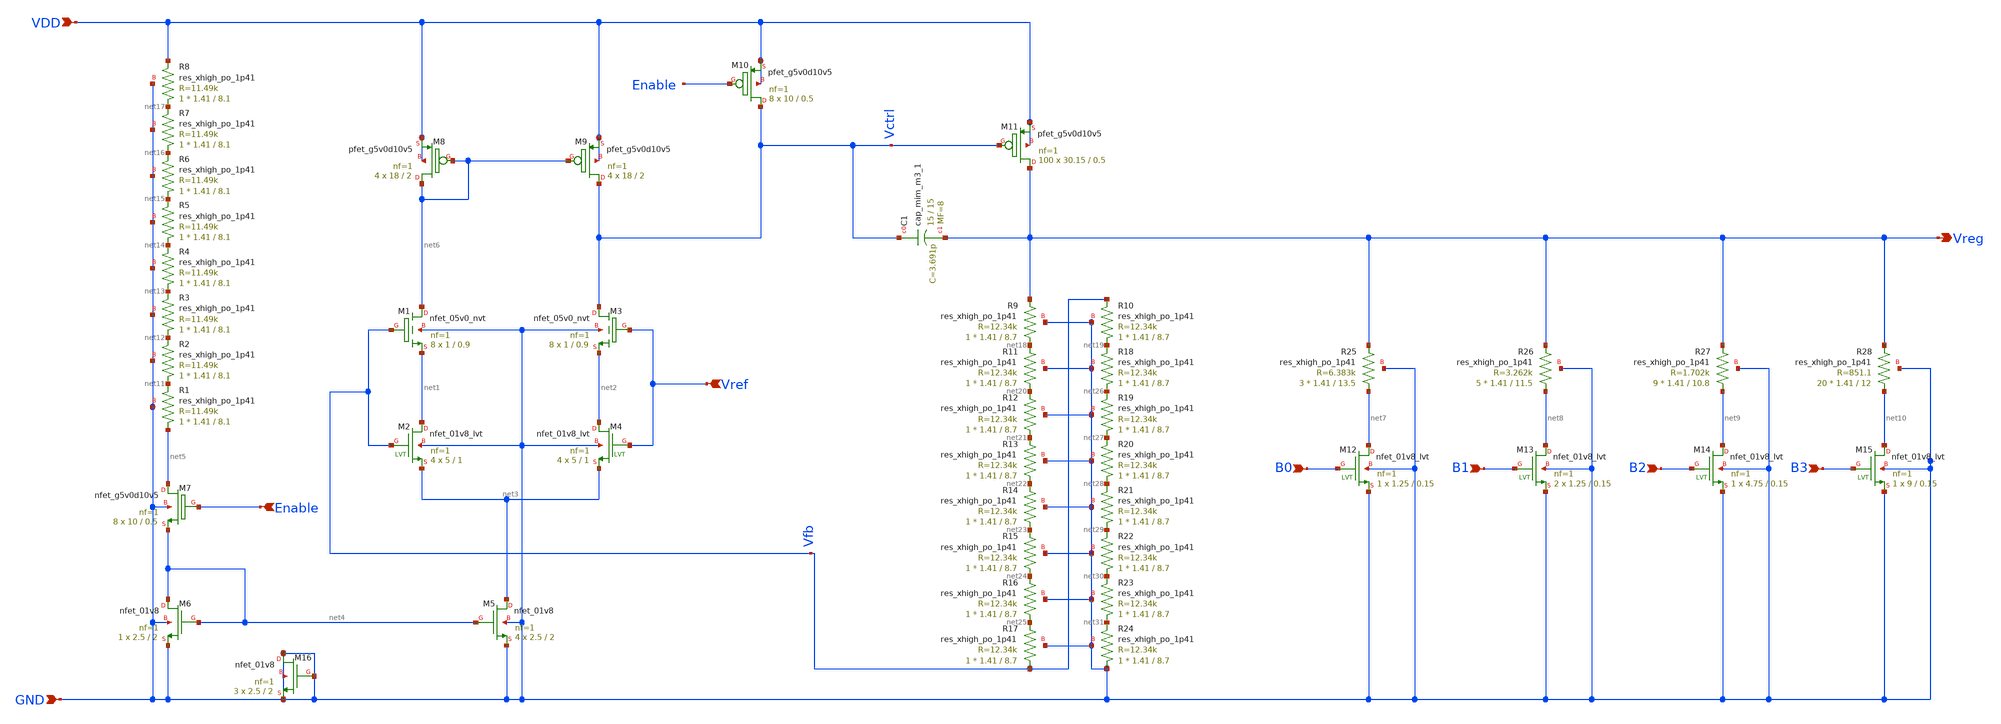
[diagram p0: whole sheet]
** sch_path: ALDO/ALDO.sch
**.subckt ALDO Vref Enable B0 B1 B2 B3 VDD GND Vreg
*.ipin Vref
*.ipin Enable
*.ipin B0
*.ipin B1
*.ipin B2
*.ipin B3
*.ipin VDD
*.ipin GND
*.opin Vreg
XM1 net6 Vfb net1 GND sky130_fd_pr__nfet_05v0_nvt L=0.9 W=1 nf=1 ad='int((nf+1)/2) * W/nf * 0.29' as='int((nf+2)/2) * W/nf * 0.29'
+ pd='2*int((nf+1)/2) * (W/nf + 0.29)' ps='2*int((nf+2)/2) * (W/nf + 0.29)' nrd='0.29 / W' nrs='0.29 / W'
+ sa=0 sb=0 sd=0 mult=8 m=8
XM2 net1 Vfb net3 GND sky130_fd_pr__nfet_01v8_lvt L=1 W=5 nf=1 ad='int((nf+1)/2) * W/nf * 0.29' as='int((nf+2)/2) * W/nf * 0.29'
+ pd='2*int((nf+1)/2) * (W/nf + 0.29)' ps='2*int((nf+2)/2) * (W/nf + 0.29)' nrd='0.29 / W' nrs='0.29 / W'
+ sa=0 sb=0 sd=0 mult=4 m=4
XM3 Vctrl Vref net2 GND sky130_fd_pr__nfet_05v0_nvt L=0.9 W=1 nf=1 ad='int((nf+1)/2) * W/nf * 0.29' as='int((nf+2)/2) * W/nf * 0.29'
+ pd='2*int((nf+1)/2) * (W/nf + 0.29)' ps='2*int((nf+2)/2) * (W/nf + 0.29)' nrd='0.29 / W' nrs='0.29 / W'
+ sa=0 sb=0 sd=0 mult=8 m=8
XM4 net2 Vref net3 GND sky130_fd_pr__nfet_01v8_lvt L=1 W=5 nf=1 ad='int((nf+1)/2) * W/nf * 0.29' as='int((nf+2)/2) * W/nf * 0.29'
+ pd='2*int((nf+1)/2) * (W/nf + 0.29)' ps='2*int((nf+2)/2) * (W/nf + 0.29)' nrd='0.29 / W' nrs='0.29 / W'
+ sa=0 sb=0 sd=0 mult=4 m=4
XM5 net3 net4 GND GND sky130_fd_pr__nfet_01v8 L=2 W=2.5 nf=1 ad='int((nf+1)/2) * W/nf * 0.29' as='int((nf+2)/2) * W/nf * 0.29'
+ pd='2*int((nf+1)/2) * (W/nf + 0.29)' ps='2*int((nf+2)/2) * (W/nf + 0.29)' nrd='0.29 / W' nrs='0.29 / W'
+ sa=0 sb=0 sd=0 mult=4 m=4
XM6 net4 net4 GND GND sky130_fd_pr__nfet_01v8 L=2 W=2.5 nf=1 ad='int((nf+1)/2) * W/nf * 0.29' as='int((nf+2)/2) * W/nf * 0.29'
+ pd='2*int((nf+1)/2) * (W/nf + 0.29)' ps='2*int((nf+2)/2) * (W/nf + 0.29)' nrd='0.29 / W' nrs='0.29 / W'
+ sa=0 sb=0 sd=0 mult=1 m=1
XM7 net5 Enable net4 GND sky130_fd_pr__nfet_g5v0d10v5 L=0.5 W=10 nf=1 ad='int((nf+1)/2) * W/nf * 0.29'
+ as='int((nf+2)/2) * W/nf * 0.29' pd='2*int((nf+1)/2) * (W/nf + 0.29)' ps='2*int((nf+2)/2) * (W/nf + 0.29)'
+ nrd='0.29 / W' nrs='0.29 / W' sa=0 sb=0 sd=0 mult=8 m=8
XR1 net5 net11 GND sky130_fd_pr__res_xhigh_po_1p41 L=8.1 mult=1 m=1
XR2 net11 net12 GND sky130_fd_pr__res_xhigh_po_1p41 L=8.1 mult=1 m=1
XR3 net12 net13 GND sky130_fd_pr__res_xhigh_po_1p41 L=8.1 mult=1 m=1
XR4 net13 net14 GND sky130_fd_pr__res_xhigh_po_1p41 L=8.1 mult=1 m=1
XR5 net14 net15 GND sky130_fd_pr__res_xhigh_po_1p41 L=8.1 mult=1 m=1
XR6 net15 net16 GND sky130_fd_pr__res_xhigh_po_1p41 L=8.1 mult=1 m=1
XR7 net16 net17 GND sky130_fd_pr__res_xhigh_po_1p41 L=8.1 mult=1 m=1
XR8 net17 VDD GND sky130_fd_pr__res_xhigh_po_1p41 L=8.1 mult=1 m=1
XM8 net6 net6 VDD VDD sky130_fd_pr__pfet_g5v0d10v5 L=2 W=18 nf=1 ad='int((nf+1)/2) * W/nf * 0.29' as='int((nf+2)/2) * W/nf * 0.29'
+ pd='2*int((nf+1)/2) * (W/nf + 0.29)' ps='2*int((nf+2)/2) * (W/nf + 0.29)' nrd='0.29 / W' nrs='0.29 / W'
+ sa=0 sb=0 sd=0 mult=4 m=4
XM9 Vctrl net6 VDD VDD sky130_fd_pr__pfet_g5v0d10v5 L=2 W=18 nf=1 ad='int((nf+1)/2) * W/nf * 0.29' as='int((nf+2)/2) * W/nf * 0.29'
+ pd='2*int((nf+1)/2) * (W/nf + 0.29)' ps='2*int((nf+2)/2) * (W/nf + 0.29)' nrd='0.29 / W' nrs='0.29 / W'
+ sa=0 sb=0 sd=0 mult=4 m=4
XM10 Vctrl Enable VDD VDD sky130_fd_pr__pfet_g5v0d10v5 L=0.5 W=10 nf=1 ad='int((nf+1)/2) * W/nf * 0.29'
+ as='int((nf+2)/2) * W/nf * 0.29' pd='2*int((nf+1)/2) * (W/nf + 0.29)' ps='2*int((nf+2)/2) * (W/nf + 0.29)'
+ nrd='0.29 / W' nrs='0.29 / W' sa=0 sb=0 sd=0 mult=8 m=8
XM11 Vreg Vctrl VDD VDD sky130_fd_pr__pfet_g5v0d10v5 L=0.5 W=30.15 nf=1 ad='int((nf+1)/2) * W/nf * 0.29'
+ as='int((nf+2)/2) * W/nf * 0.29' pd='2*int((nf+1)/2) * (W/nf + 0.29)' ps='2*int((nf+2)/2) * (W/nf + 0.29)'
+ nrd='0.29 / W' nrs='0.29 / W' sa=0 sb=0 sd=0 mult=100 m=100
XC1 Vctrl Vreg sky130_fd_pr__cap_mim_m3_1 W=15 L=15 MF=8 m=8
XR9 net18 Vreg GND sky130_fd_pr__res_xhigh_po_1p41 L=8.7 mult=1 m=1
XR10 net19 Vfb GND sky130_fd_pr__res_xhigh_po_1p41 L=8.7 mult=1 m=1
XR25 net7 Vreg GND sky130_fd_pr__res_xhigh_po_1p41 L=13.5 mult=3 m=3
XM12 net7 B0 GND GND sky130_fd_pr__nfet_01v8_lvt L=0.15 W=1.25 nf=1 ad='int((nf+1)/2) * W/nf * 0.29'
+ as='int((nf+2)/2) * W/nf * 0.29' pd='2*int((nf+1)/2) * (W/nf + 0.29)' ps='2*int((nf+2)/2) * (W/nf + 0.29)'
+ nrd='0.29 / W' nrs='0.29 / W' sa=0 sb=0 sd=0 mult=1 m=1
XR26 net8 Vreg GND sky130_fd_pr__res_xhigh_po_1p41 L=11.5 mult=5 m=5
XM13 net8 B1 GND GND sky130_fd_pr__nfet_01v8_lvt L=0.15 W=1.25 nf=1 ad='int((nf+1)/2) * W/nf * 0.29'
+ as='int((nf+2)/2) * W/nf * 0.29' pd='2*int((nf+1)/2) * (W/nf + 0.29)' ps='2*int((nf+2)/2) * (W/nf + 0.29)'
+ nrd='0.29 / W' nrs='0.29 / W' sa=0 sb=0 sd=0 mult=2 m=2
XR27 net9 Vreg GND sky130_fd_pr__res_xhigh_po_1p41 L=10.8 mult=9 m=9
XM14 net9 B2 GND GND sky130_fd_pr__nfet_01v8_lvt L=0.15 W=4.75 nf=1 ad='int((nf+1)/2) * W/nf * 0.29'
+ as='int((nf+2)/2) * W/nf * 0.29' pd='2*int((nf+1)/2) * (W/nf + 0.29)' ps='2*int((nf+2)/2) * (W/nf + 0.29)'
+ nrd='0.29 / W' nrs='0.29 / W' sa=0 sb=0 sd=0 mult=1 m=1
XR28 net10 Vreg GND sky130_fd_pr__res_xhigh_po_1p41 L=12 mult=20 m=20
XM15 net10 B3 GND GND sky130_fd_pr__nfet_01v8_lvt L=0.15 W=9 nf=1 ad='int((nf+1)/2) * W/nf * 0.29' as='int((nf+2)/2) * W/nf * 0.29'
+ pd='2*int((nf+1)/2) * (W/nf + 0.29)' ps='2*int((nf+2)/2) * (W/nf + 0.29)' nrd='0.29 / W' nrs='0.29 / W'
+ sa=0 sb=0 sd=0 mult=1 m=1
XR11 net20 net18 GND sky130_fd_pr__res_xhigh_po_1p41 L=8.7 mult=1 m=1
XR12 net21 net20 GND sky130_fd_pr__res_xhigh_po_1p41 L=8.7 mult=1 m=1
XR13 net22 net21 GND sky130_fd_pr__res_xhigh_po_1p41 L=8.7 mult=1 m=1
XR14 net23 net22 GND sky130_fd_pr__res_xhigh_po_1p41 L=8.7 mult=1 m=1
XR15 net24 net23 GND sky130_fd_pr__res_xhigh_po_1p41 L=8.7 mult=1 m=1
XR16 net25 net24 GND sky130_fd_pr__res_xhigh_po_1p41 L=8.7 mult=1 m=1
XR17 Vfb net25 GND sky130_fd_pr__res_xhigh_po_1p41 L=8.7 mult=1 m=1
XR18 net26 net19 GND sky130_fd_pr__res_xhigh_po_1p41 L=8.7 mult=1 m=1
XR19 net27 net26 GND sky130_fd_pr__res_xhigh_po_1p41 L=8.7 mult=1 m=1
XR20 net28 net27 GND sky130_fd_pr__res_xhigh_po_1p41 L=8.7 mult=1 m=1
XR21 net29 net28 GND sky130_fd_pr__res_xhigh_po_1p41 L=8.7 mult=1 m=1
XR22 net30 net29 GND sky130_fd_pr__res_xhigh_po_1p41 L=8.7 mult=1 m=1
XR23 net31 net30 GND sky130_fd_pr__res_xhigh_po_1p41 L=8.7 mult=1 m=1
XR24 GND net31 GND sky130_fd_pr__res_xhigh_po_1p41 L=8.7 mult=1 m=1
XM16 GND GND GND GND sky130_fd_pr__nfet_01v8 L=2 W=2.5 nf=1 ad='int((nf+1)/2) * W/nf * 0.29' as='int((nf+2)/2) * W/nf * 0.29'
+ pd='2*int((nf+1)/2) * (W/nf + 0.29)' ps='2*int((nf+2)/2) * (W/nf + 0.29)' nrd='0.29 / W' nrs='0.29 / W'
+ sa=0 sb=0 sd=0 mult=3 m=3
**.ends
.end
